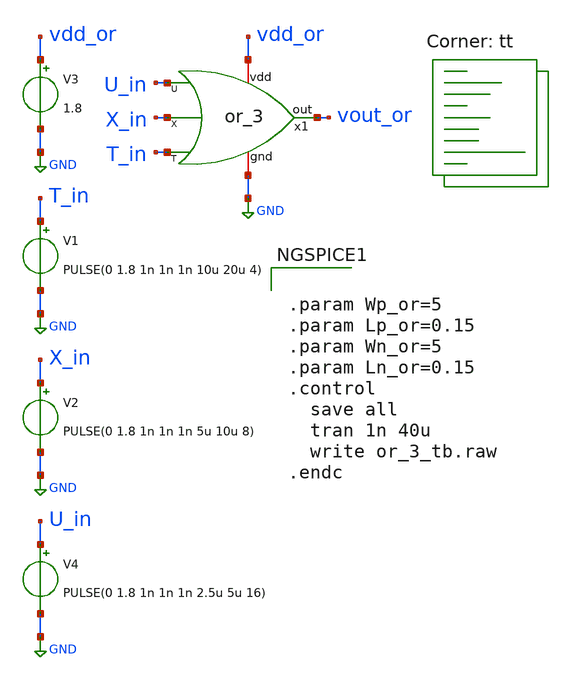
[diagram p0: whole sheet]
** sch_path: inhibitory/or_3_tb.sch
**.subckt or_3_tb
V1 T_in GND PULSE(0 1.8 1n 1n 1n 10u 20u 4)
V3 vdd_or GND 1.8
V2 X_in GND PULSE(0 1.8 1n 1n 1n 5u 10u 8)
x1 U_in X_in T_in vdd_or vout_or GND or_3
V4 U_in GND PULSE(0 1.8 1n 1n 1n 2.5u 5u 16)
**** begin user architecture code
.lib $::SKYWATER_MODELS/sky130.lib.spice tt


.param Wp_or=5
.param Lp_or=0.15
.param Wn_or=5
.param Ln_or=0.15
.control
  save all
  tran 1n 40u
  write or_3_tb.raw
.endc

**** end user architecture code
**.ends
.GLOBAL GND
.end
